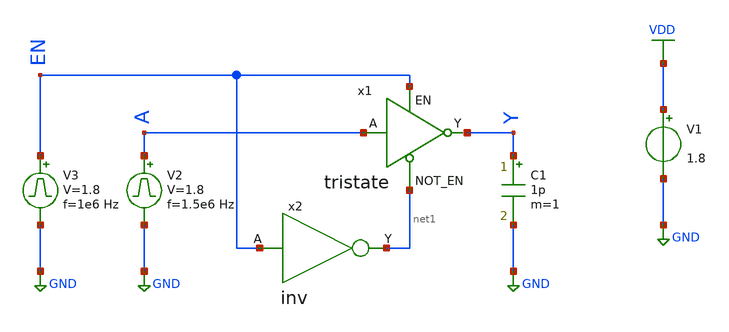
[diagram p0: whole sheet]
** sch_path: library/xschem/tristate_tb.sch
**.subckt tristate_tb
V1 VDD GND 1.8
V2 A GND pulse 0 1.8 '0.495/ 1.5e6 ' '0.01/1.5e6 ' '0.01/1.5e6 ' '0.49/1.5e6 ' '1/1.5e6 '
C1 Y GND 1p m=1
V3 EN GND pulse 0 1.8 '0.495/ 1e6 ' '0.01/1e6 ' '0.01/1e6 ' '0.49/1e6 ' '1/1e6 '
x1 A net1 Y EN tristate
x2 EN net1 inv
**** begin user architecture code


.control
save all
tran 1n 2u
plot V(A) V(EN)+2 V(Y)+4
.endc


** opencircuitdesign pdks install
.lib $::SKYWATER_MODELS/sky130.lib.spice tt


**** end user architecture code
**.ends
.GLOBAL VDD
.GLOBAL GND
.end
